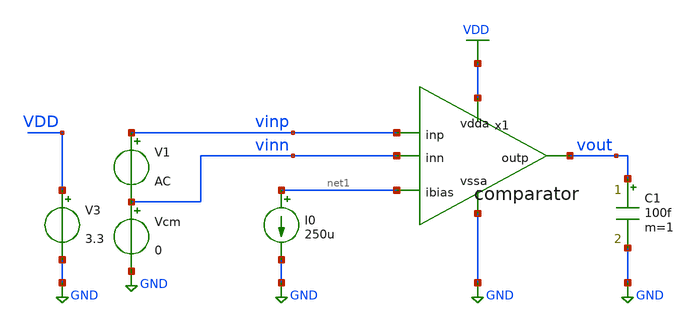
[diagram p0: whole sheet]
** sch_path: xschem/tb_comp_ac.sch
**.subckt tb_comp_ac
I0 net1 GND 250u
C1 vout GND 100f m=1
V3 VDD GND 3.3
x1 VDD net1 vinp vinn vout GND comparator
V1 vinp vinn AC
Vcm vinn GND 0
**** begin user architecture code



.lib /home/ttuser/pdk/sky130A/libs.tech/ngspice/sky130.lib.spice tt

.option temp=27

.control
  ac dec 100 0.1 100MEG
  meas ac AOL max vdb(vout)
  plot vdb(vout)
  *plot 180/PI*phase(vout)
.endc

.save all



**** end user architecture code
**.ends
.GLOBAL GND
.GLOBAL VDD
.end
